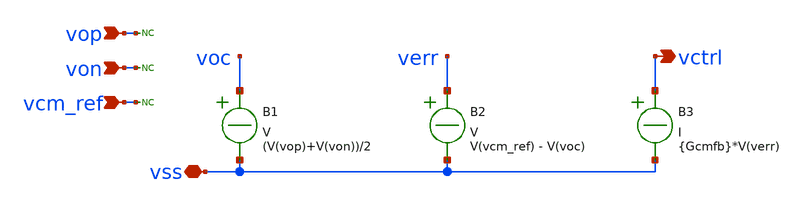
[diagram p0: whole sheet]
** sch_path: 3_real_circuits/ideal_cmfb.sch
**.subckt ideal_cmfb vctrl vop von vcm_ref vss
*.opin vctrl
*.ipin vop
*.ipin von
*.ipin vcm_ref
*.iopin vss
B1 voc vss V = (V(vop)+V(von))/2
B2 verr vss V = V(vcm_ref) - V(voc)
B3 vctrl vss I = {Gcmfb}*V(verr)
* noconn vop
* noconn von
* noconn vcm_ref
**.ends
.end
